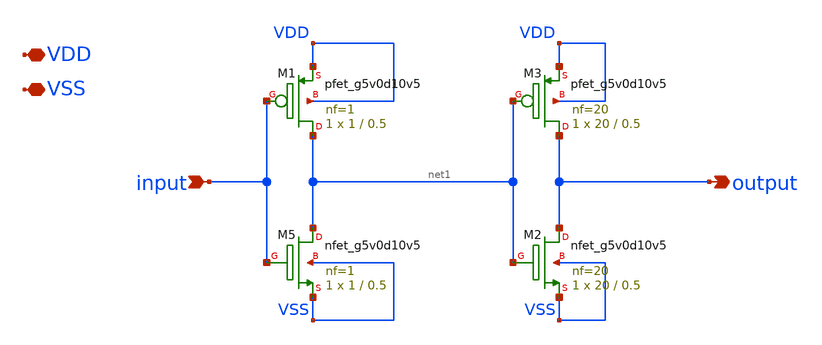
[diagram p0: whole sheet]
** sch_path: tt_um_3v_inverter_SiliconeGuide/xschem/double_inverter.sch
**.subckt double_inverter input output VDD VSS
*.ipin input
*.opin output
*.iopin VDD
*.iopin VSS
XM1 net1 input VDD VDD sky130_fd_pr__pfet_g5v0d10v5 L=0.5 W=1 nf=1 ad='int((nf+1)/2) * W/nf * 0.29' as='int((nf+2)/2) * W/nf * 0.29'
+ pd='2*int((nf+1)/2) * (W/nf + 0.29)' ps='2*int((nf+2)/2) * (W/nf + 0.29)' nrd='0.29 / W' nrs='0.29 / W'
+ sa=0 sb=0 sd=0 mult=1 m=1
XM3 output net1 VDD VDD sky130_fd_pr__pfet_g5v0d10v5 L=0.5 W=20 nf=20 ad='int((nf+1)/2) * W/nf * 0.29'
+ as='int((nf+2)/2) * W/nf * 0.29' pd='2*int((nf+1)/2) * (W/nf + 0.29)' ps='2*int((nf+2)/2) * (W/nf + 0.29)'
+ nrd='0.29 / W' nrs='0.29 / W' sa=0 sb=0 sd=0 mult=1 m=1
XM5 net1 input VSS VSS sky130_fd_pr__nfet_g5v0d10v5 L=0.5 W=1 nf=1 ad='int((nf+1)/2) * W/nf * 0.29' as='int((nf+2)/2) * W/nf * 0.29'
+ pd='2*int((nf+1)/2) * (W/nf + 0.29)' ps='2*int((nf+2)/2) * (W/nf + 0.29)' nrd='0.29 / W' nrs='0.29 / W'
+ sa=0 sb=0 sd=0 mult=1 m=1
XM2 output net1 VSS VSS sky130_fd_pr__nfet_g5v0d10v5 L=0.5 W=20 nf=20 ad='int((nf+1)/2) * W/nf * 0.29'
+ as='int((nf+2)/2) * W/nf * 0.29' pd='2*int((nf+1)/2) * (W/nf + 0.29)' ps='2*int((nf+2)/2) * (W/nf + 0.29)'
+ nrd='0.29 / W' nrs='0.29 / W' sa=0 sb=0 sd=0 mult=1 m=1
**.ends
.end
